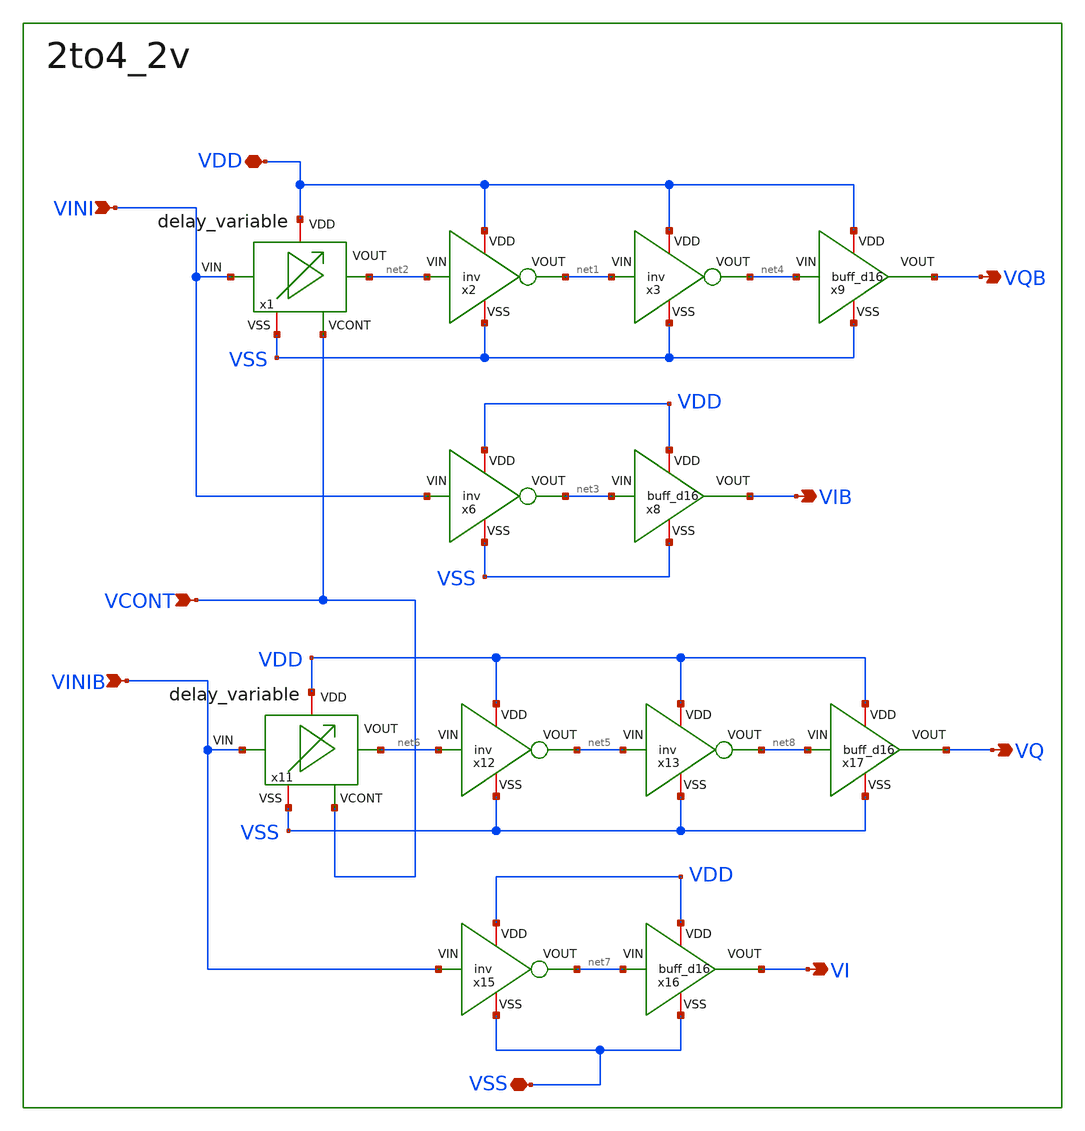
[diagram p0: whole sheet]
** sch_path: 2to4/2to4_2v.sch
**.subckt 2to4_2v VCONT VINI VIB VQ VINIB VI VQB VDD VSS
*.ipin VCONT
*.ipin VINI
*.opin VIB
*.opin VQ
*.ipin VINIB
*.opin VI
*.opin VQB
*.iopin VDD
*.iopin VSS
x1 VDD VINI net2 VCONT VSS delay_variable
x2 VDD net1 net2 VSS inv
x3 VDD net4 net1 VSS inv
x6 VDD net3 VINI VSS inv
x8 VDD VIB net3 VSS buff_d16
x9 VDD VQB net4 VSS buff_d16
x11 VDD VINIB net6 VCONT VSS delay_variable
x12 VDD net5 net6 VSS inv
x13 VDD net8 net5 VSS inv
x15 VDD net7 VINIB VSS inv
x16 VDD VI net7 VSS buff_d16
x17 VDD VQ net8 VSS buff_d16
**.ends
.end
